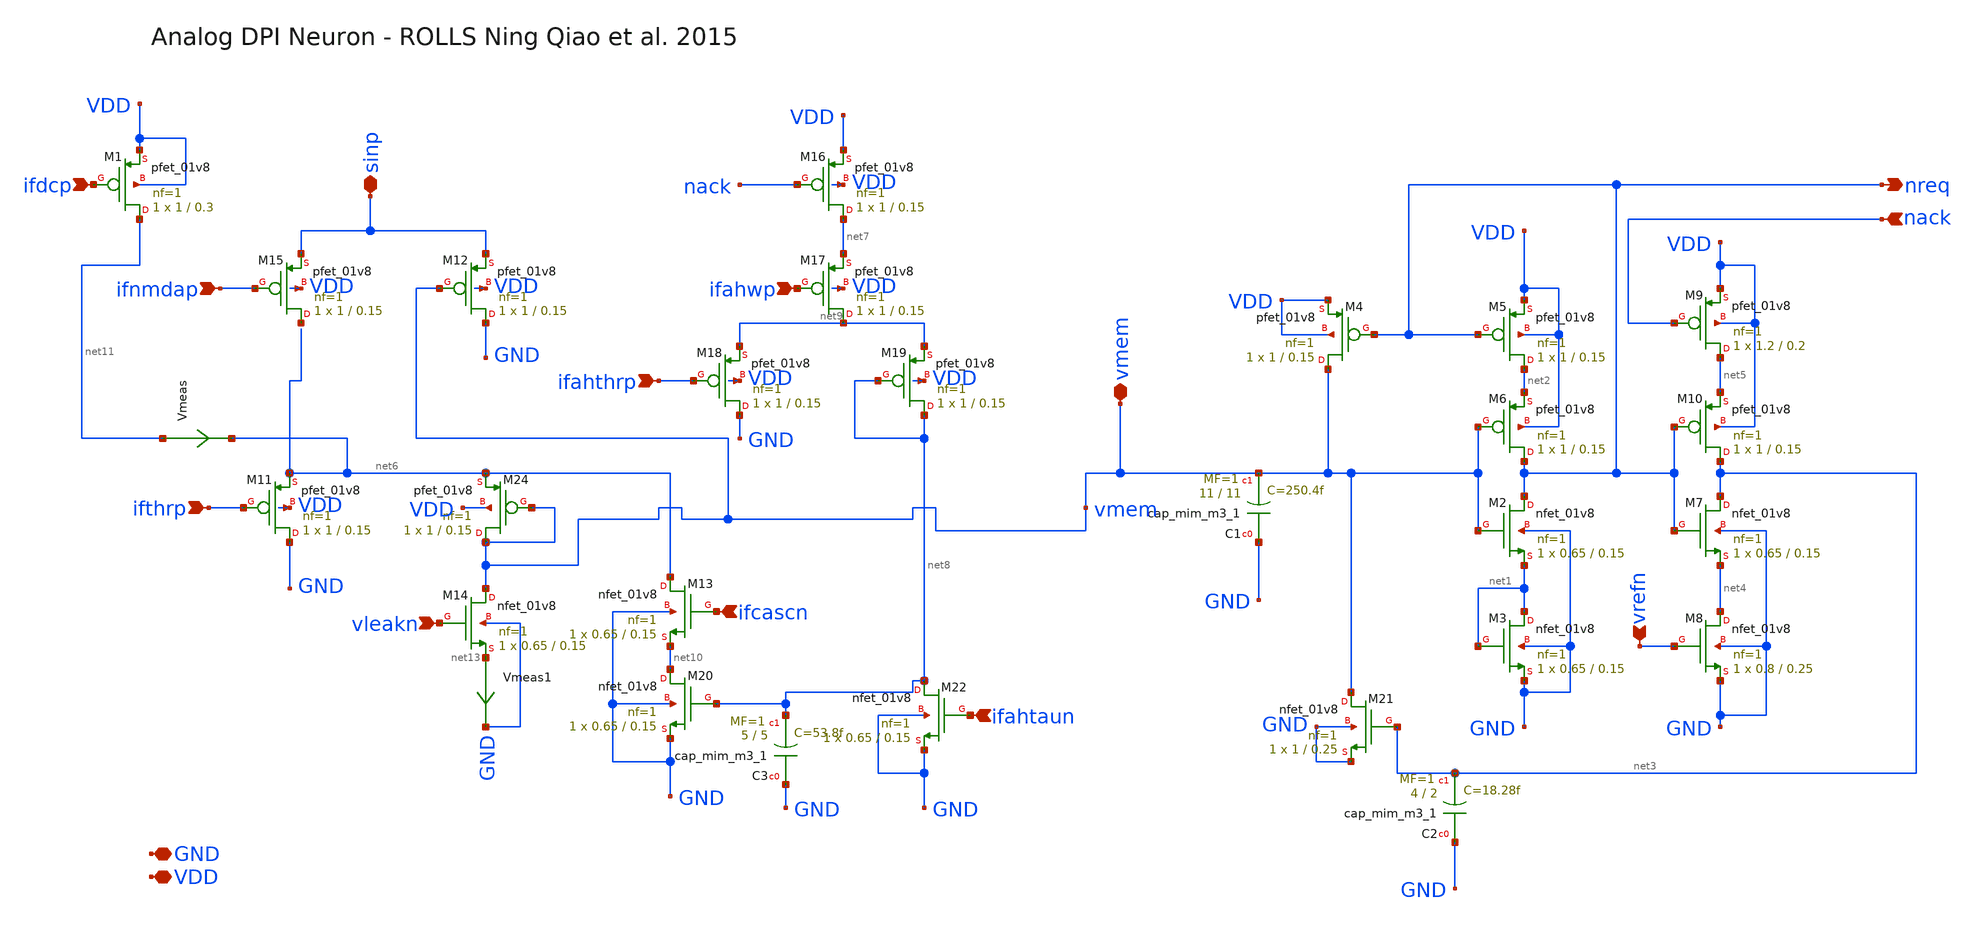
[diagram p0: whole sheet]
** sch_path: design/xschem/neuron_analog_fc.sch
**.subckt neuron_analog_fc vleakn GND VDD nreq vrefn nack ifdcp ifthrp ifnmdap ifahwp ifahthrp
*+ ifahtaun ifcascn vmem sinp
*.ipin vleakn
*.iopin GND
*.iopin VDD
*.opin nreq
*.ipin vrefn
*.ipin nack
*.ipin ifdcp
*.ipin ifthrp
*.ipin ifnmdap
*.ipin ifahwp
*.ipin ifahthrp
*.ipin ifahtaun
*.ipin ifcascn
*.iopin vmem
*.iopin sinp
XC1 GND vmem sky130_fd_pr__cap_mim_m3_1 W=11 L=11 MF=1 m=1
XM8 net4 vrefn GND GND sky130_fd_pr__nfet_01v8 L=0.25 W=0.8 nf=1 ad='int((nf+1)/2) * W/nf * 0.29' as='int((nf+2)/2) * W/nf * 0.29'
+ pd='2*int((nf+1)/2) * (W/nf + 0.29)' ps='2*int((nf+2)/2) * (W/nf + 0.29)' nrd='0.29 / W' nrs='0.29 / W'
+ sa=0 sb=0 sd=0 mult=1 m=1
XM9 net5 nack VDD VDD sky130_fd_pr__pfet_01v8 L=0.2 W=1.2 nf=1 ad='int((nf+1)/2) * W/nf * 0.29' as='int((nf+2)/2) * W/nf * 0.29'
+ pd='2*int((nf+1)/2) * (W/nf + 0.29)' ps='2*int((nf+2)/2) * (W/nf + 0.29)' nrd='0.29 / W' nrs='0.29 / W'
+ sa=0 sb=0 sd=0 mult=1 m=1
XC2 GND net3 sky130_fd_pr__cap_mim_m3_1 W=4 L=2 MF=1 m=1
XM21 vmem net3 GND GND sky130_fd_pr__nfet_01v8 L=0.25 W=1 nf=1 ad='int((nf+1)/2) * W/nf * 0.29' as='int((nf+2)/2) * W/nf * 0.29'
+ pd='2*int((nf+1)/2) * (W/nf + 0.29)' ps='2*int((nf+2)/2) * (W/nf + 0.29)' nrd='0.29 / W' nrs='0.29 / W'
+ sa=0 sb=0 sd=0 mult=1 m=1
XM15 net12 ifnmdap sinp VDD sky130_fd_pr__pfet_01v8 L=0.15 W=1 nf=1 ad='int((nf+1)/2) * W/nf * 0.29'
+ as='int((nf+2)/2) * W/nf * 0.29' pd='2*int((nf+1)/2) * (W/nf + 0.29)' ps='2*int((nf+2)/2) * (W/nf + 0.29)'
+ nrd='0.29 / W' nrs='0.29 / W' sa=0 sb=0 sd=0 mult=1 m=1
XC3 GND net8 sky130_fd_pr__cap_mim_m3_1 W=5 L=5 MF=1 m=1
XM12 GND vmem sinp VDD sky130_fd_pr__pfet_01v8 L=0.15 W=1 nf=1 ad='int((nf+1)/2) * W/nf * 0.29' as='int((nf+2)/2) * W/nf * 0.29'
+ pd='2*int((nf+1)/2) * (W/nf + 0.29)' ps='2*int((nf+2)/2) * (W/nf + 0.29)' nrd='0.29 / W' nrs='0.29 / W'
+ sa=0 sb=0 sd=0 mult=1 m=1
XM11 GND ifthrp net6 VDD sky130_fd_pr__pfet_01v8 L=0.15 W=1 nf=1 ad='int((nf+1)/2) * W/nf * 0.29' as='int((nf+2)/2) * W/nf * 0.29'
+ pd='2*int((nf+1)/2) * (W/nf + 0.29)' ps='2*int((nf+2)/2) * (W/nf + 0.29)' nrd='0.29 / W' nrs='0.29 / W'
+ sa=0 sb=0 sd=0 mult=1 m=1
XM16 net7 nack VDD VDD sky130_fd_pr__pfet_01v8 L=0.15 W=1 nf=1 ad='int((nf+1)/2) * W/nf * 0.29' as='int((nf+2)/2) * W/nf * 0.29'
+ pd='2*int((nf+1)/2) * (W/nf + 0.29)' ps='2*int((nf+2)/2) * (W/nf + 0.29)' nrd='0.29 / W' nrs='0.29 / W'
+ sa=0 sb=0 sd=0 mult=1 m=1
XM17 net9 ifahwp net7 VDD sky130_fd_pr__pfet_01v8 L=0.15 W=1 nf=1 ad='int((nf+1)/2) * W/nf * 0.29' as='int((nf+2)/2) * W/nf * 0.29'
+ pd='2*int((nf+1)/2) * (W/nf + 0.29)' ps='2*int((nf+2)/2) * (W/nf + 0.29)' nrd='0.29 / W' nrs='0.29 / W'
+ sa=0 sb=0 sd=0 mult=1 m=1
XM18 GND ifahthrp net9 VDD sky130_fd_pr__pfet_01v8 L=0.15 W=1 nf=1 ad='int((nf+1)/2) * W/nf * 0.29' as='int((nf+2)/2) * W/nf * 0.29'
+ pd='2*int((nf+1)/2) * (W/nf + 0.29)' ps='2*int((nf+2)/2) * (W/nf + 0.29)' nrd='0.29 / W' nrs='0.29 / W'
+ sa=0 sb=0 sd=0 mult=1 m=1
XM19 net8 net8 net9 VDD sky130_fd_pr__pfet_01v8 L=0.15 W=1 nf=1 ad='int((nf+1)/2) * W/nf * 0.29' as='int((nf+2)/2) * W/nf * 0.29'
+ pd='2*int((nf+1)/2) * (W/nf + 0.29)' ps='2*int((nf+2)/2) * (W/nf + 0.29)' nrd='0.29 / W' nrs='0.29 / W'
+ sa=0 sb=0 sd=0 mult=1 m=1
XM1 net11 ifdcp VDD VDD sky130_fd_pr__pfet_01v8 L=0.3 W=1 nf=1 ad='int((nf+1)/2) * W/nf * 0.29' as='int((nf+2)/2) * W/nf * 0.29'
+ pd='2*int((nf+1)/2) * (W/nf + 0.29)' ps='2*int((nf+2)/2) * (W/nf + 0.29)' nrd='0.29 / W' nrs='0.29 / W'
+ sa=0 sb=0 sd=0 mult=1 m=1
XM5 net2 nreq VDD VDD sky130_fd_pr__pfet_01v8 L=0.15 W=1 nf=1 ad='int((nf+1)/2) * W/nf * 0.29' as='int((nf+2)/2) * W/nf * 0.29'
+ pd='2*int((nf+1)/2) * (W/nf + 0.29)' ps='2*int((nf+2)/2) * (W/nf + 0.29)' nrd='0.29 / W' nrs='0.29 / W'
+ sa=0 sb=0 sd=0 mult=1 m=1
XM6 nreq vmem net2 VDD sky130_fd_pr__pfet_01v8 L=0.15 W=1 nf=1 ad='int((nf+1)/2) * W/nf * 0.29' as='int((nf+2)/2) * W/nf * 0.29'
+ pd='2*int((nf+1)/2) * (W/nf + 0.29)' ps='2*int((nf+2)/2) * (W/nf + 0.29)' nrd='0.29 / W' nrs='0.29 / W'
+ sa=0 sb=0 sd=0 mult=1 m=1
XM10 net3 nreq net5 VDD sky130_fd_pr__pfet_01v8 L=0.15 W=1 nf=1 ad='int((nf+1)/2) * W/nf * 0.29' as='int((nf+2)/2) * W/nf * 0.29'
+ pd='2*int((nf+1)/2) * (W/nf + 0.29)' ps='2*int((nf+2)/2) * (W/nf + 0.29)' nrd='0.29 / W' nrs='0.29 / W'
+ sa=0 sb=0 sd=0 mult=1 m=1
XM2 nreq vmem net1 GND sky130_fd_pr__nfet_01v8 L=0.15 W=0.65 nf=1 ad='int((nf+1)/2) * W/nf * 0.29' as='int((nf+2)/2) * W/nf * 0.29'
+ pd='2*int((nf+1)/2) * (W/nf + 0.29)' ps='2*int((nf+2)/2) * (W/nf + 0.29)' nrd='0.29 / W' nrs='0.29 / W'
+ sa=0 sb=0 sd=0 mult=1 m=1
XM3 net1 net1 GND GND sky130_fd_pr__nfet_01v8 L=0.15 W=0.65 nf=1 ad='int((nf+1)/2) * W/nf * 0.29' as='int((nf+2)/2) * W/nf * 0.29'
+ pd='2*int((nf+1)/2) * (W/nf + 0.29)' ps='2*int((nf+2)/2) * (W/nf + 0.29)' nrd='0.29 / W' nrs='0.29 / W'
+ sa=0 sb=0 sd=0 mult=1 m=1
XM7 net3 nreq net4 GND sky130_fd_pr__nfet_01v8 L=0.15 W=0.65 nf=1 ad='int((nf+1)/2) * W/nf * 0.29' as='int((nf+2)/2) * W/nf * 0.29'
+ pd='2*int((nf+1)/2) * (W/nf + 0.29)' ps='2*int((nf+2)/2) * (W/nf + 0.29)' nrd='0.29 / W' nrs='0.29 / W'
+ sa=0 sb=0 sd=0 mult=1 m=1
XM14 vmem vleakn net13 GND sky130_fd_pr__nfet_01v8 L=0.15 W=0.65 nf=1 ad='int((nf+1)/2) * W/nf * 0.29'
+ as='int((nf+2)/2) * W/nf * 0.29' pd='2*int((nf+1)/2) * (W/nf + 0.29)' ps='2*int((nf+2)/2) * (W/nf + 0.29)'
+ nrd='0.29 / W' nrs='0.29 / W' sa=0 sb=0 sd=0 mult=1 m=1
XM4 vmem nreq VDD VDD sky130_fd_pr__pfet_01v8 L=0.15 W=1 nf=1 ad='int((nf+1)/2) * W/nf * 0.29' as='int((nf+2)/2) * W/nf * 0.29'
+ pd='2*int((nf+1)/2) * (W/nf + 0.29)' ps='2*int((nf+2)/2) * (W/nf + 0.29)' nrd='0.29 / W' nrs='0.29 / W'
+ sa=0 sb=0 sd=0 mult=1 m=1
XM24 vmem vmem net6 VDD sky130_fd_pr__pfet_01v8 L=0.15 W=1 nf=1 ad='int((nf+1)/2) * W/nf * 0.29' as='int((nf+2)/2) * W/nf * 0.29'
+ pd='2*int((nf+1)/2) * (W/nf + 0.29)' ps='2*int((nf+2)/2) * (W/nf + 0.29)' nrd='0.29 / W' nrs='0.29 / W'
+ sa=0 sb=0 sd=0 mult=1 m=1
Vmeas net11 net6 0
.save i(vmeas)
Vmeas1 net13 GND 0
.save i(vmeas1)
XM13 net6 ifcascn net10 GND sky130_fd_pr__nfet_01v8 L=0.15 W=0.65 nf=1 ad='int((nf+1)/2) * W/nf * 0.29'
+ as='int((nf+2)/2) * W/nf * 0.29' pd='2*int((nf+1)/2) * (W/nf + 0.29)' ps='2*int((nf+2)/2) * (W/nf + 0.29)'
+ nrd='0.29 / W' nrs='0.29 / W' sa=0 sb=0 sd=0 mult=1 m=1
XM20 net10 net8 GND GND sky130_fd_pr__nfet_01v8 L=0.15 W=0.65 nf=1 ad='int((nf+1)/2) * W/nf * 0.29' as='int((nf+2)/2) * W/nf * 0.29'
+ pd='2*int((nf+1)/2) * (W/nf + 0.29)' ps='2*int((nf+2)/2) * (W/nf + 0.29)' nrd='0.29 / W' nrs='0.29 / W'
+ sa=0 sb=0 sd=0 mult=1 m=1
XM22 net8 ifahtaun GND GND sky130_fd_pr__nfet_01v8 L=0.15 W=0.65 nf=1 ad='int((nf+1)/2) * W/nf * 0.29'
+ as='int((nf+2)/2) * W/nf * 0.29' pd='2*int((nf+1)/2) * (W/nf + 0.29)' ps='2*int((nf+2)/2) * (W/nf + 0.29)'
+ nrd='0.29 / W' nrs='0.29 / W' sa=0 sb=0 sd=0 mult=1 m=1
**.ends
.end
